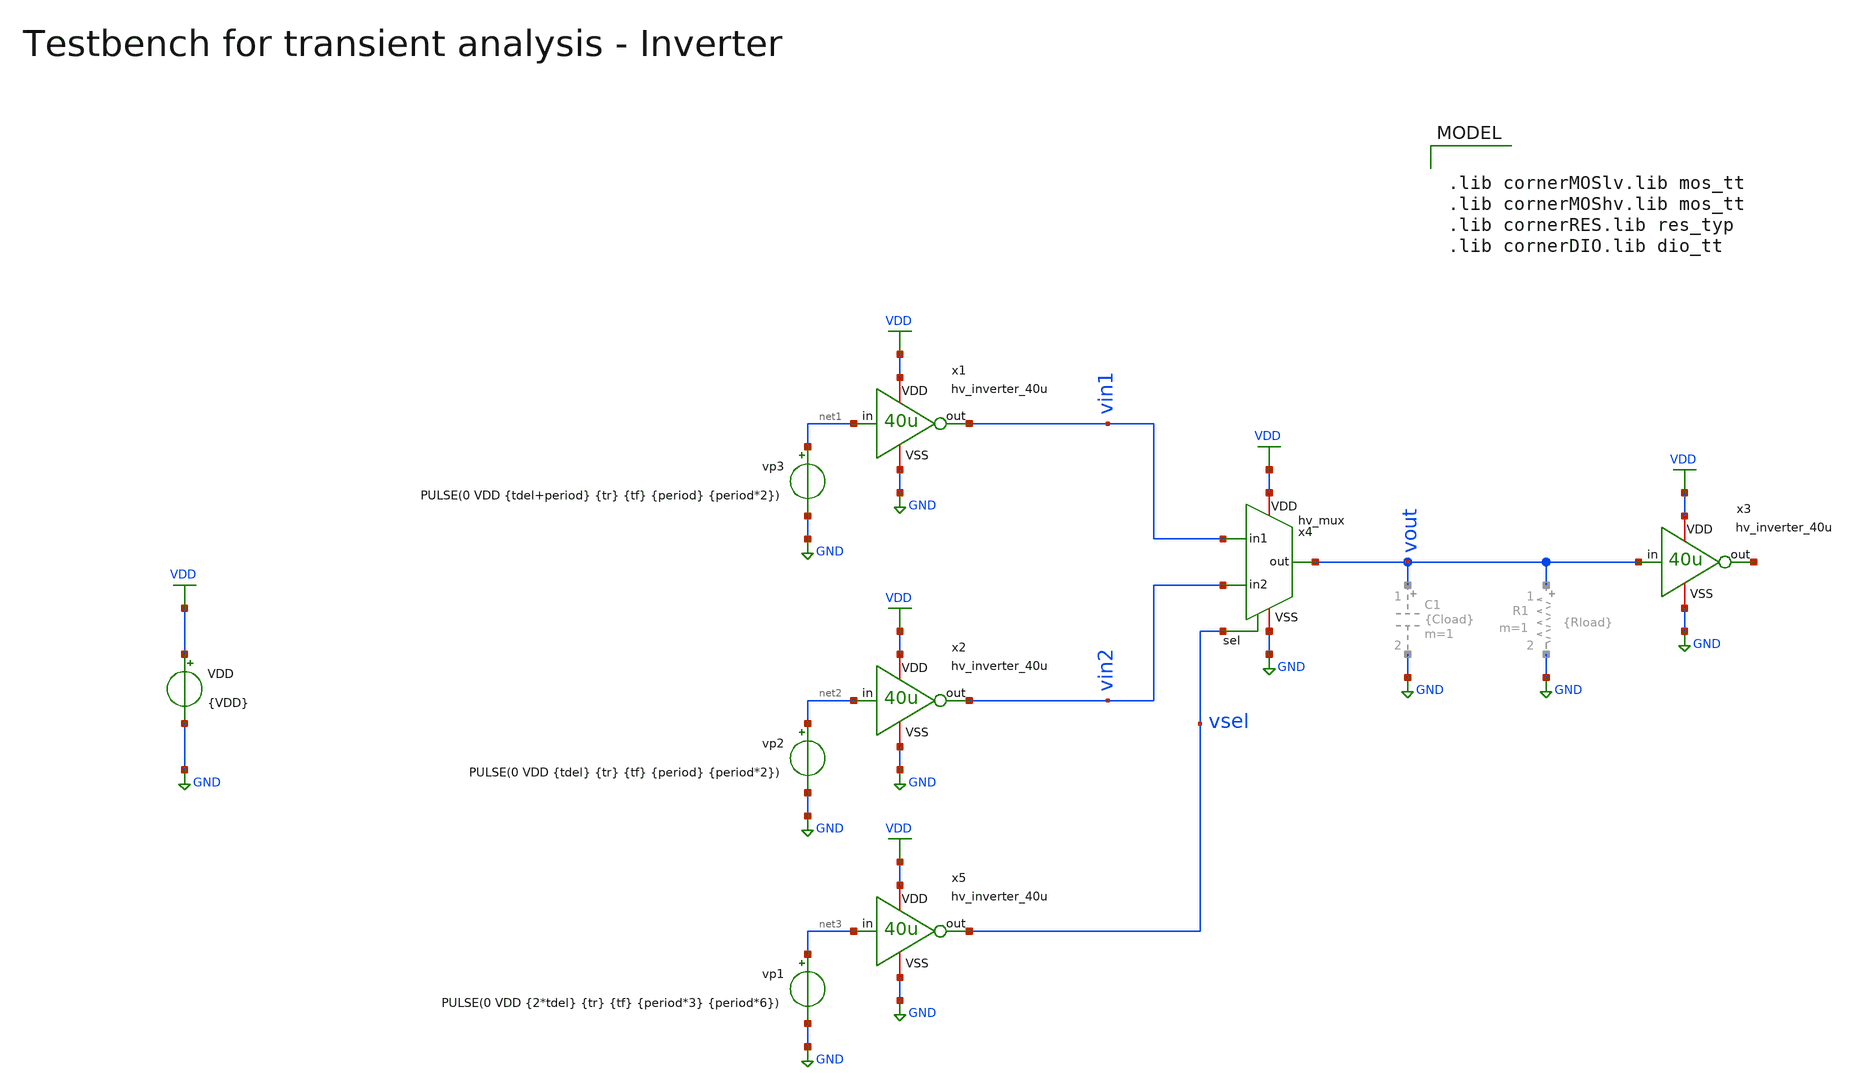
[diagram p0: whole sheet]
** sch_path: macros/heichips26_vcr/macros/switched_capacitor/testbenches/xschem/tb_hv_mux_tran.sch
**.subckt tb_hv_mux_tran
VDD VDD GND {VDD}
vp2 net2 GND PULSE(0 VDD {tdel} {tr} {tf} {period} {period*2})
vp1 net3 GND PULSE(0 VDD {2*tdel} {tr} {tf} {period*3} {period*6})
x1 VDD net1 vin1 GND hv_inverter_40u
x2 VDD net2 vin2 GND hv_inverter_40u
x3 VDD vout net4 GND hv_inverter_40u
x4 vsel vin1 VDD vout GND vin2 hv_mux
vp3 net1 GND PULSE(0 VDD {tdel+period} {tr} {tf} {period} {period*2})
x5 VDD net3 vsel GND hv_inverter_40u
**** begin user architecture code


.param VDD=3.3
.csparam VDD=VDD
.param Vcm=VDD/2
.param temp=27
.param Cload=10p
.param Rload=1k

.param period = 1n
.param tdel   = {period/2}
.param ton    = {period*2}
.csparam tstop  = {12*period}
.csparam tstep  = {period/100}
.param tr     = {period/100}
.param tf     = {period/100}

.options savecurrents klu method=gear reltol=1e-4 abstol=1e-15 gmin=1e-15
.control

save all

* Operating Point Analysis
op
remzerovec
write @schname\.raw
set appendwrite

* Transient Analysis
tran {$&tstep} {$&tstop}
write @schname\.raw

* Plotting
plot vsel+12 vin1+8 vin2+4 vout

* Write Data
unset appendwrite
set wr_vecnames
set wr_singlescale
wrdata ../plot_simulations/data/@schname\.txt v(vin1) v(vin2) v(vout)

*quit
.endc



.lib cornerMOSlv.lib mos_tt
.lib cornerMOShv.lib mos_tt
.lib cornerRES.lib res_typ
.lib cornerDIO.lib dio_tt

**** end user architecture code
**.ends

* expanding   symbol:  hv_inverter_40u.sym # of pins=4
** sym_path: macros/heichips26_vcr/macros/switched_capacitor/schematic/xschem/hv_inverter_40u.sym
** sch_path: macros/heichips26_vcr/macros/switched_capacitor/schematic/xschem/hv_inverter_40u.sch
.subckt hv_inverter_40u VDD in out VSS
*.ipin in
*.iopin VDD
*.iopin VSS
*.opin out
XM2 out in VSS VSS sg13_hv_nmos w={n_w} l={n_l} ng={ng} m=1 mm_ok=1
XM3 out in VDD VDD sg13_hv_pmos w={p_w} l={p_l} ng={ng} m=1 mm_ok=1
**** begin user architecture code


.param w   = 10u
.param ng  = 4
.param n_ng = ng
.param n_w = {3u*n_ng}
.param n_l = 0.45u
.param p_ng = ng
.param p_w = {10u*p_ng}
.param p_l = 0.4u


**** end user architecture code
.ends


* expanding   symbol:  hv_mux.sym # of pins=6
** sym_path: macros/heichips26_vcr/macros/switched_capacitor/schematic/xschem/hv_mux.sym
** sch_path: macros/heichips26_vcr/macros/switched_capacitor/schematic/xschem/hv_mux.sch
.subckt hv_mux sel in1 VDD out VSS in2
*.ipin in1
*.iopin VDD
*.iopin VSS
*.opin out
*.ipin in2
*.ipin sel
x3 VDD sel net3 VSS hv_inverter_40u
x1 VDD in1 net2 sel VSS hv_nor
x2 VDD in2 net1 net3 VSS hv_nor
x4 VDD net2 out net1 VSS hv_nor
.ends


* expanding   symbol:  hv_nor.sym # of pins=5
** sym_path: macros/heichips26_vcr/macros/switched_capacitor/schematic/xschem/hv_nor.sym
** sch_path: macros/heichips26_vcr/macros/switched_capacitor/schematic/xschem/hv_nor.sch
.subckt hv_nor VDD in1 out in2 VSS
*.ipin in1
*.iopin VDD
*.iopin VSS
*.opin out
*.ipin in2
**** begin user architecture code


.param w   = 10u
.param ng  = 4
.param n_ng = ng
.param n_w = {3u*n_ng}
.param n_l = 0.45u
.param p_ng = ng
.param p_w = {10u*p_ng}
.param p_l = 0.4u


**** end user architecture code
XM2 out in1 VSS VSS sg13_hv_nmos w={n_w} l={n_l} ng={ng} m=1 mm_ok=1
XM3 net1 in2 VDD VDD sg13_hv_pmos w={p_w} l={p_l} ng={ng} m=1 mm_ok=1
XM1 out in2 VSS VSS sg13_hv_nmos w={n_w} l={n_l} ng={ng} m=1 mm_ok=1
XM4 out in1 net1 VDD sg13_hv_pmos w={p_w} l={p_l} ng={ng} m=1 mm_ok=1
.ends

.GLOBAL GND
.GLOBAL VDD
.end
